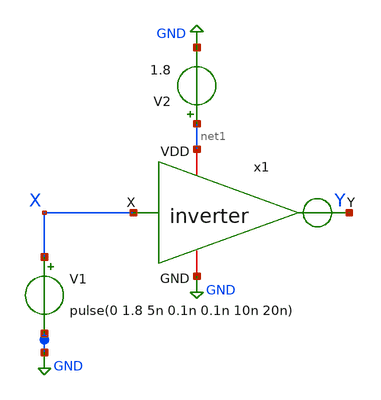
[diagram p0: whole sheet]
** sch_path: Layouts and Schematics/Spice Sim and Schem/invtest.sch
**.subckt invtest
x1 net1 X Y GND inv
V1 X GND pulse(0 1.8 5n 0.1n 0.1n 10n 20n)
V2 net1 GND 1.8
**** begin user architecture code
 .lib $::SKYWATER_MODELS/sky130.lib.spice tt

.tran 1n 40n
.control
run
.endc

**** end user architecture code
**.ends

* expanding   symbol:  inv.sym # of pins=4
** sym_path: Layouts and Schematics/Spice Sim and Schem/inv.sym
** sch_path: Layouts and Schematics/Spice Sim and Schem/inv.sch
.subckt inv VDD X Y GND
*.ipin X
*.iopin VDD
*.iopin GND
*.opin Y
XM1 Y X GND GND sky130_fd_pr__nfet_01v8 L=0.5 W=1 nf=1 ad='int((nf+1)/2) * W/nf * 0.29' as='int((nf+2)/2) * W/nf * 0.29'
+ pd='2*int((nf+1)/2) * (W/nf + 0.29)' ps='2*int((nf+2)/2) * (W/nf + 0.29)' nrd='0.29 / W' nrs='0.29 / W'
+ sa=0 sb=0 sd=0 mult=1 m=1
XM2 Y X VDD VDD sky130_fd_pr__pfet_01v8 L=0.5 W=2 nf=1 ad='int((nf+1)/2) * W/nf * 0.29' as='int((nf+2)/2) * W/nf * 0.29'
+ pd='2*int((nf+1)/2) * (W/nf + 0.29)' ps='2*int((nf+2)/2) * (W/nf + 0.29)' nrd='0.29 / W' nrs='0.29 / W'
+ sa=0 sb=0 sd=0 mult=1 m=1
.ends

.GLOBAL GND
.end
